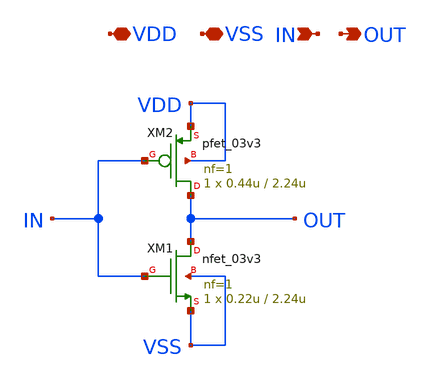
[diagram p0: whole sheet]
** sch_path: SCOP_INPUT_AND_MUX_PAKISTAN_03/Xschem/Logic_Gates/INV_16x.sch
**.subckt INV_16x VDD VSS IN OUT
*.iopin VDD
*.iopin VSS
*.ipin IN
*.opin OUT
XM1 OUT IN VSS VSS nfet_03v3 L=2.24u W=0.22u nf=1 ad='int((nf+1)/2) * W/nf * 0.18u' as='int((nf+2)/2) * W/nf * 0.18u'
+ pd='2*int((nf+1)/2) * (W/nf + 0.18u)' ps='2*int((nf+2)/2) * (W/nf + 0.18u)' nrd='0.18u / W' nrs='0.18u / W'
+ sa=0 sb=0 sd=0 m=1
XM2 OUT IN VDD VDD pfet_03v3 L=2.24u W=0.44u nf=1 ad='int((nf+1)/2) * W/nf * 0.18u' as='int((nf+2)/2) * W/nf * 0.18u'
+ pd='2*int((nf+1)/2) * (W/nf + 0.18u)' ps='2*int((nf+2)/2) * (W/nf + 0.18u)' nrd='0.18u / W' nrs='0.18u / W'
+ sa=0 sb=0 sd=0 m=1
**.ends
.end
